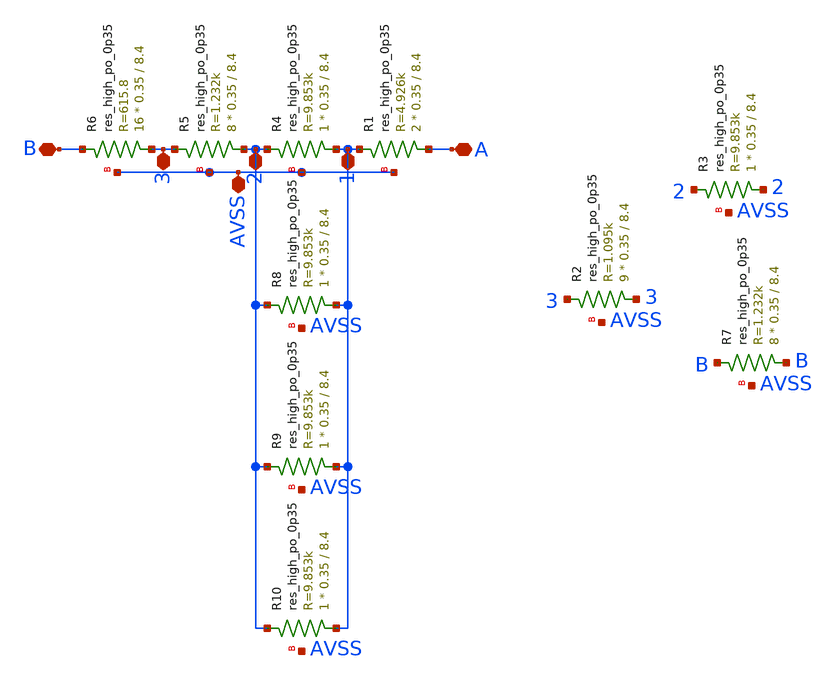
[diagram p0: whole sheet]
** sch_path: magic/res_trim.sch
**.subckt res_trim B A AVSS 1 2 3
*.iopin B
*.iopin A
*.iopin AVSS
*.iopin 1
*.iopin 2
*.iopin 3
XR1 A 1 AVSS sky130_fd_pr__res_high_po_0p35 L=8.4 mult=2 m=2
XR4 1 2 AVSS sky130_fd_pr__res_high_po_0p35 L=8.4 mult=1 m=1
XR5 2 3 AVSS sky130_fd_pr__res_high_po_0p35 L=8.4 mult=8 m=8
XR6 3 B AVSS sky130_fd_pr__res_high_po_0p35 L=8.4 mult=16 m=16
XR8 1 2 AVSS sky130_fd_pr__res_high_po_0p35 L=8.4 mult=1 m=1
XR9 1 2 AVSS sky130_fd_pr__res_high_po_0p35 L=8.4 mult=1 m=1
XR10 1 2 AVSS sky130_fd_pr__res_high_po_0p35 L=8.4 mult=1 m=1
XR2 3 3 AVSS sky130_fd_pr__res_high_po_0p35 L=8.4 mult=9 m=9
XR3 2 2 AVSS sky130_fd_pr__res_high_po_0p35 L=8.4 mult=1 m=1
XR7 B B AVSS sky130_fd_pr__res_high_po_0p35 L=8.4 mult=8 m=8
**.ends
.end
